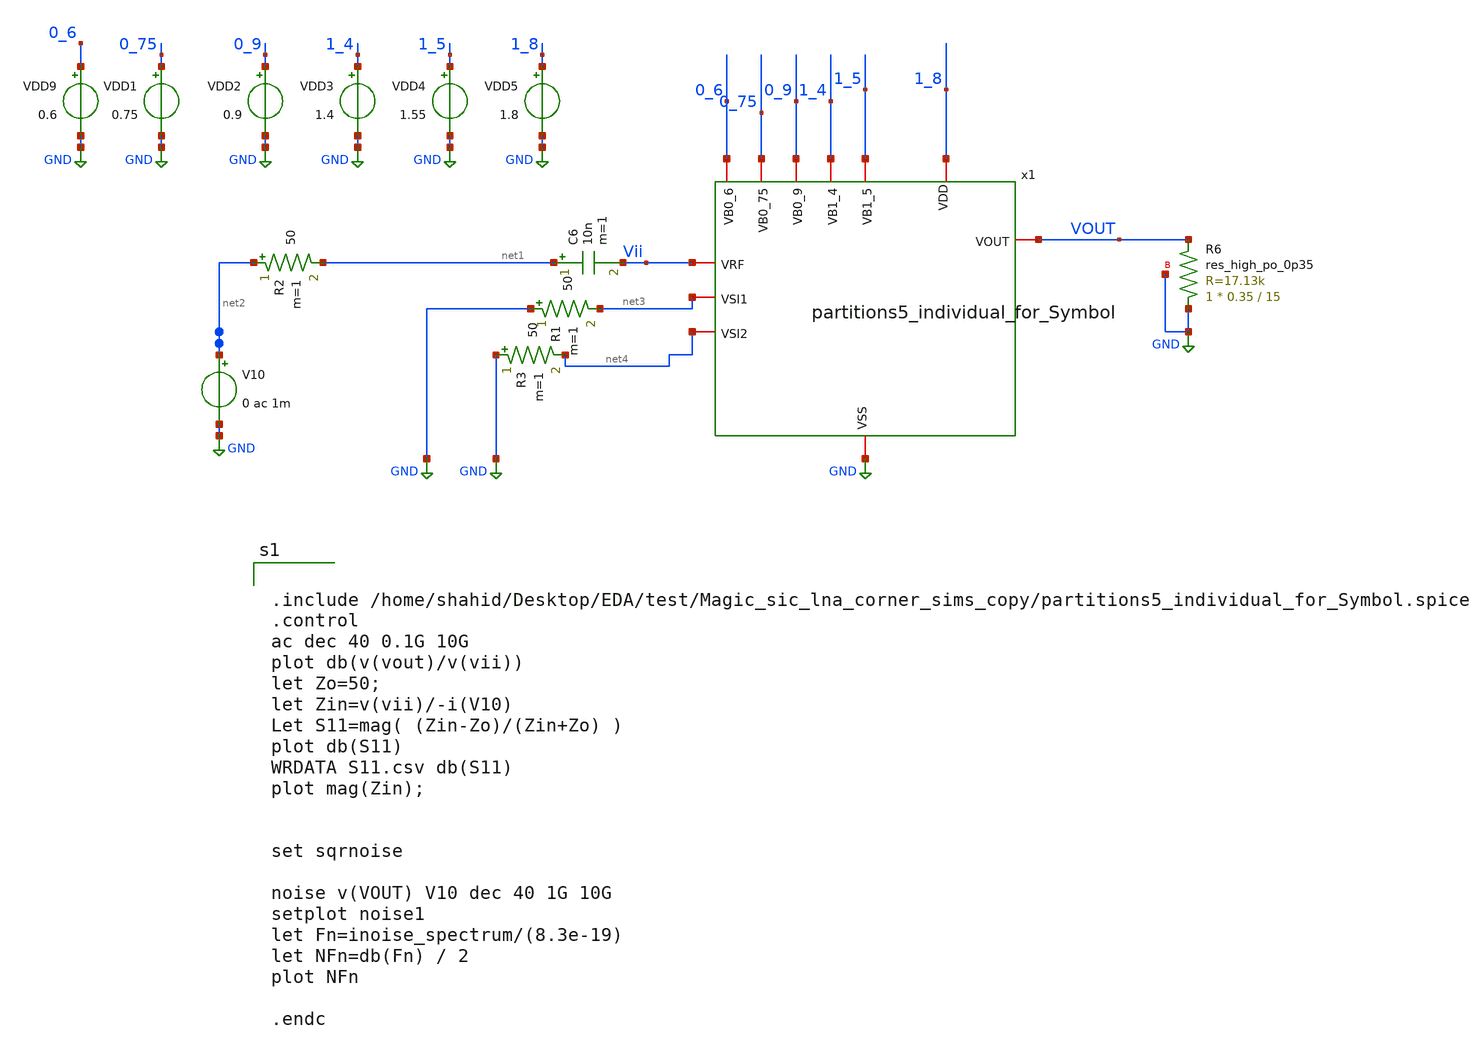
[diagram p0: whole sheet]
** sch_path: xschem/xschem4_sic_oct_20/TB.sch
**.subckt TB
x1 1_8 0_6 VOUT net4 1_5 0_9 1_4 Vii net3 0_75 GND partitions5_individual_for_Symbol
VDD9 0_6 GND 0.6
VDD1 0_75 GND 0.75
VDD2 0_9 GND 0.9
VDD3 1_4 GND 1.4
VDD4 1_5 GND 1.55
VDD5 1_8 GND 1.8
C6 net1 Vii 10n m=1
V10 net2 GND 0 ac 1m
R2 net2 net1 50 m=1
R1 GND net3 50 m=1
R3 GND net4 50 m=1
XR6 GND VOUT GND sky130_fd_pr__res_high_po_0p35 L=15 mult=1 m=1
**** begin user architecture code


.include /home/shahid/Desktop/EDA/test/Magic_sic_lna_corner_sims_copy/partitions5_individual_for_Symbol.spice
.control
ac dec 40 0.1G 10G
plot db(v(vout)/v(vii))
let Zo=50;
let Zin=v(vii)/-i(V10)
Let S11=mag( (Zin-Zo)/(Zin+Zo) )
plot db(S11)
WRDATA S11.csv db(S11)
plot mag(Zin);


set sqrnoise

noise v(VOUT) V10 dec 40 1G 10G
setplot noise1
let Fn=inoise_spectrum/(8.3e-19)
let NFn=db(Fn) / 2
plot NFn

.endc



.lib $::SKYWATER_MODELS/sky130.lib.spice ff

**** end user architecture code
**.ends

* expanding   symbol:  partitions5_individual_for_Symbol.sym # of pins=11
** sym_path: xschem/xschem4_sic_oct_20/partitions5_individual_for_Symbol.sym
** sch_path: xschem/xschem4_sic_oct_20/partitions5_individual_for_Symbol.sch
.subckt partitions5_individual_for_Symbol VDD VB0_6 VOUT VSI2 VB1_5 VB0_9 VB1_4 VRF VSI1 VB0_75 VSS
*.iopin VRF
*.iopin VSS
*.iopin VB0_75
*.iopin VSI1
*.iopin VB1_4
*.iopin VDD
*.iopin VB1_5
*.iopin VB0_9
*.iopin VSI2
*.iopin VB0_6
*.iopin VOUT
XM12 net1 VRF VSS VSS sky130_fd_pr__nfet_01v8_lvt L=0.15 W=220 nf=22 ad='int((nf+1)/2) * W/nf * 0.29'
+ as='int((nf+2)/2) * W/nf * 0.29' pd='2*int((nf+1)/2) * (W/nf + 0.29)' ps='2*int((nf+2)/2) * (W/nf + 0.29)'
+ nrd='0.29 / W' nrs='0.29 / W' sa=0 sb=0 sd=0 mult=1 m=1
XM13 net1 VRF VDD VDD sky130_fd_pr__pfet_01v8 L=0.15 W=30 nf=3 ad='int((nf+1)/2) * W/nf * 0.29' as='int((nf+2)/2) * W/nf * 0.29'
+ pd='2*int((nf+1)/2) * (W/nf + 0.29)' ps='2*int((nf+2)/2) * (W/nf + 0.29)' nrd='0.29 / W' nrs='0.29 / W'
+ sa=0 sb=0 sd=0 mult=1 m=1
XM14 VOUT1 VB1_4 net1 VSS sky130_fd_pr__nfet_01v8_lvt L=0.15 W=80 nf=8 ad='int((nf+1)/2) * W/nf * 0.29'
+ as='int((nf+2)/2) * W/nf * 0.29' pd='2*int((nf+1)/2) * (W/nf + 0.29)' ps='2*int((nf+2)/2) * (W/nf + 0.29)'
+ nrd='0.29 / W' nrs='0.29 / W' sa=0 sb=0 sd=0 mult=1 m=1
XM16 VRF VB0_75 VSS VSS sky130_fd_pr__nfet_01v8_lvt L=0.15 W=7.8 nf=1 ad='int((nf+1)/2) * W/nf * 0.29'
+ as='int((nf+2)/2) * W/nf * 0.29' pd='2*int((nf+1)/2) * (W/nf + 0.29)' ps='2*int((nf+2)/2) * (W/nf + 0.29)'
+ nrd='0.29 / W' nrs='0.29 / W' sa=0 sb=0 sd=0 mult=1 m=1
XM20 net1 VSI1 VSS VSS sky130_fd_pr__nfet_01v8_lvt L=0.15 W=240 nf=24 ad='int((nf+1)/2) * W/nf * 0.29'
+ as='int((nf+2)/2) * W/nf * 0.29' pd='2*int((nf+1)/2) * (W/nf + 0.29)' ps='2*int((nf+2)/2) * (W/nf + 0.29)'
+ nrd='0.29 / W' nrs='0.29 / W' sa=0 sb=0 sd=0 mult=1 m=1
XR16 VB0_75 VSI1 VSS sky130_fd_pr__res_high_po_0p35 L=6.2 mult=1 m=1
XR4 VB1_5 net2 VSS sky130_fd_pr__res_high_po_0p35 L=4 mult=1 m=1
XC5 net2 VOUT1 sky130_fd_pr__cap_mim_m3_2 W=30 L=30 MF=1 m=1
XM15 net3 net2 VRF VSS sky130_fd_pr__nfet_01v8_lvt L=0.15 W=7.8 nf=1 ad='int((nf+1)/2) * W/nf * 0.29'
+ as='int((nf+2)/2) * W/nf * 0.29' pd='2*int((nf+1)/2) * (W/nf + 0.29)' ps='2*int((nf+2)/2) * (W/nf + 0.29)'
+ nrd='0.29 / W' nrs='0.29 / W' sa=0 sb=0 sd=0 mult=1 m=1
XR14 net3 VDD VSS sky130_fd_pr__res_high_po_0p35 L=0.5 mult=1 m=1
XR15 VOUT1 VDD VSS sky130_fd_pr__res_high_po_0p69 L=0.69 mult=8 m=8
XM21 VOUT2 VOUT1 VSS VSS sky130_fd_pr__nfet_01v8_lvt L=0.15 W=7.8 nf=1 ad='int((nf+1)/2) * W/nf * 0.29'
+ as='int((nf+2)/2) * W/nf * 0.29' pd='2*int((nf+1)/2) * (W/nf + 0.29)' ps='2*int((nf+2)/2) * (W/nf + 0.29)'
+ nrd='0.29 / W' nrs='0.29 / W' sa=0 sb=0 sd=0 mult=1 m=1
XR17 VOUT2 VDD VSS sky130_fd_pr__res_high_po_0p35 L=0.5 mult=1 m=1
XM17 net5 net6 VSS VSS sky130_fd_pr__nfet_01v8_lvt L=0.15 W=45 nf=7 ad='int((nf+1)/2) * W/nf * 0.29'
+ as='int((nf+2)/2) * W/nf * 0.29' pd='2*int((nf+1)/2) * (W/nf + 0.29)' ps='2*int((nf+2)/2) * (W/nf + 0.29)'
+ nrd='0.29 / W' nrs='0.29 / W' sa=0 sb=0 sd=0 mult=1 m=1
XM18 VDD net4 net5 VSS sky130_fd_pr__nfet_01v8_lvt L=0.15 W=12 nf=3 ad='int((nf+1)/2) * W/nf * 0.29'
+ as='int((nf+2)/2) * W/nf * 0.29' pd='2*int((nf+1)/2) * (W/nf + 0.29)' ps='2*int((nf+2)/2) * (W/nf + 0.29)'
+ nrd='0.29 / W' nrs='0.29 / W' sa=0 sb=0 sd=0 mult=1 m=1
XR11 net4 VDD VSS sky130_fd_pr__res_high_po_0p35 L=15 mult=1 m=1
XC7 VOUT2 net4 sky130_fd_pr__cap_mim_m3_2 W=30 L=30 MF=1 m=1
XR12 VB0_9 net6 VSS sky130_fd_pr__res_high_po_0p35 L=8 mult=1 m=1
XC8 VOUT1 net6 sky130_fd_pr__cap_mim_m3_2 W=30 L=30 MF=1 m=1
XD1 VSS net4 sky130_fd_pr__diode_pw2nd_05v5 area=1e12 pj=4e6
XM19 net5 net7 VDD VDD sky130_fd_pr__pfet_01v8 L=0.15 W=30 nf=3 ad='int((nf+1)/2) * W/nf * 0.29' as='int((nf+2)/2) * W/nf * 0.29'
+ pd='2*int((nf+1)/2) * (W/nf + 0.29)' ps='2*int((nf+2)/2) * (W/nf + 0.29)' nrd='0.29 / W' nrs='0.29 / W'
+ sa=0 sb=0 sd=0 mult=1 m=1
XR13 VB0_6 net7 VSS sky130_fd_pr__res_high_po_0p35 L=6.2 mult=1 m=1
XM22 net5 VSI2 VSS VSS sky130_fd_pr__nfet_01v8_lvt L=0.15 W=80 nf=8 ad='int((nf+1)/2) * W/nf * 0.29'
+ as='int((nf+2)/2) * W/nf * 0.29' pd='2*int((nf+1)/2) * (W/nf + 0.29)' ps='2*int((nf+2)/2) * (W/nf + 0.29)'
+ nrd='0.29 / W' nrs='0.29 / W' sa=0 sb=0 sd=0 mult=1 m=1
XR18 VB0_75 VSI2 VSS sky130_fd_pr__res_high_po_0p35 L=0.5 mult=1 m=1
XM4 VDD net8 VOUT VSS sky130_fd_pr__nfet_01v8_lvt L=0.15 W=100 nf=10 ad='int((nf+1)/2) * W/nf * 0.29'
+ as='int((nf+2)/2) * W/nf * 0.29' pd='2*int((nf+1)/2) * (W/nf + 0.29)' ps='2*int((nf+2)/2) * (W/nf + 0.29)'
+ nrd='0.29 / W' nrs='0.29 / W' sa=0 sb=0 sd=0 mult=1 m=1
XR5 net8 VDD VSS sky130_fd_pr__res_high_po_0p35 L=4 mult=1 m=1
XR6 VSS VOUT VSS sky130_fd_pr__res_high_po_0p35 L=15 mult=1 m=1
XC3 net5 net8 sky130_fd_pr__cap_mim_m3_2 W=30 L=30 MF=1 m=1
.ends

.GLOBAL GND
.end
